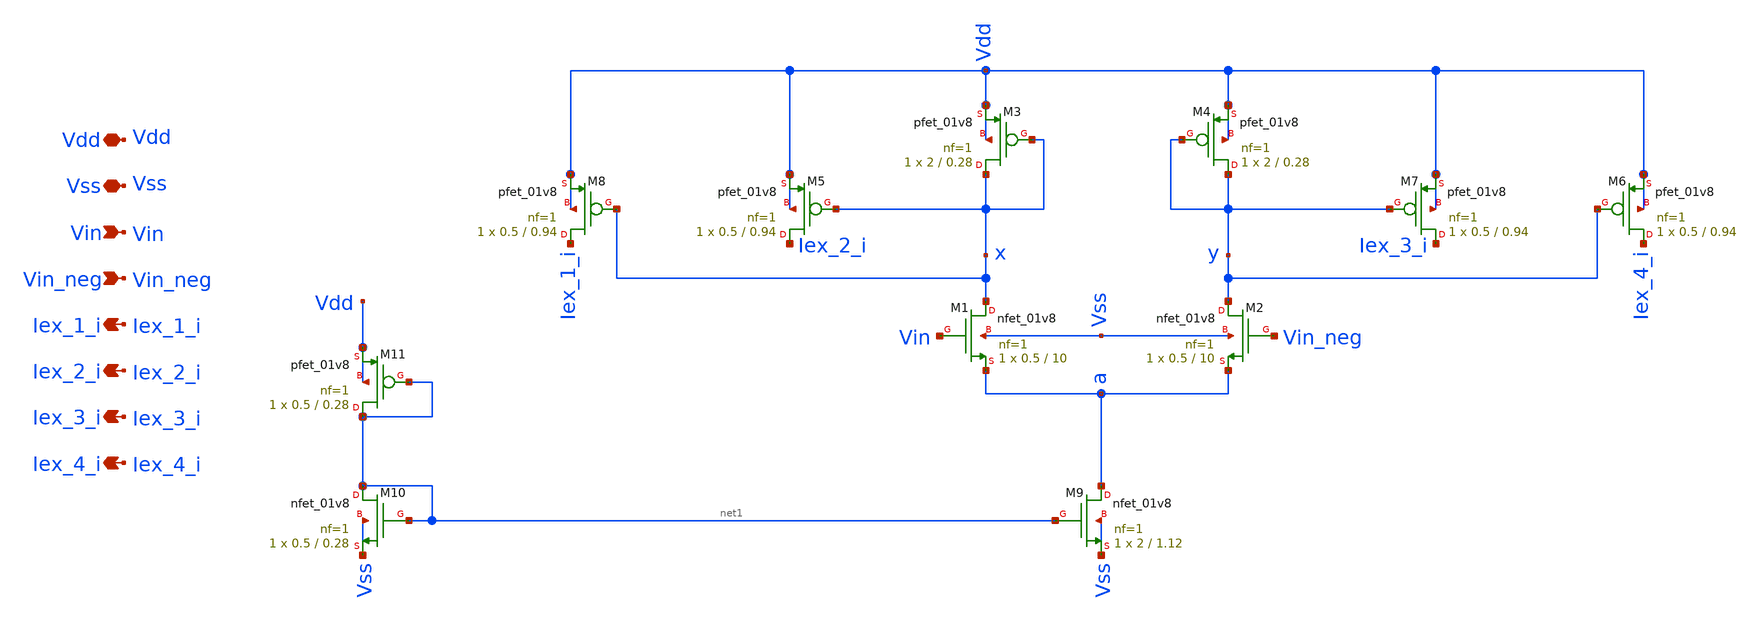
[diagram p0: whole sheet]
** sch_path: designs/libs/snn_analog/encoder/sch/encoder.sch
**.subckt encoder Vdd Vss Vin Vin_neg Iex_1_i Iex_4_i Iex_2_i Iex_3_i
*.iopin Vdd
*.iopin Vss
*.ipin Vin
*.ipin Vin_neg
*.opin Iex_1_i
*.opin Iex_4_i
*.opin Iex_2_i
*.opin Iex_3_i
XM1 x Vin a Vss sky130_fd_pr__nfet_01v8 L=10 W=0.5 nf=1 ad='int((1 + 1)/2) * 0.5 / 1 * 0.29' as='int((1 + 2)/2) * 0.5 / 1 * 0.29'
+ pd='2*int((1 + 1)/2) * (0.5 / 1 + 0.29)' ps='2*int((1 + 2)/2) * (0.5 / 1 + 0.29)' nrd='0.29 / 0.5 ' nrs='0.29 / 0.5 '
+ sa=0 sb=0 sd=0 mult=1 m=1
XM2 y Vin_neg a Vss sky130_fd_pr__nfet_01v8 L=10 W=0.5 nf=1 ad='int((1 + 1)/2) * 0.5 / 1 * 0.29' as='int((1 + 2)/2) * 0.5 / 1 * 0.29'
+ pd='2*int((1 + 1)/2) * (0.5 / 1 + 0.29)' ps='2*int((1 + 2)/2) * (0.5 / 1 + 0.29)' nrd='0.29 / 0.5 ' nrs='0.29 / 0.5 '
+ sa=0 sb=0 sd=0 mult=1 m=1
XM3 x x Vdd Vdd sky130_fd_pr__pfet_01v8 L=0.28 W=2 nf=1 ad='int((1 + 1)/2) * 2 / 1 * 0.29' as='int((1 + 2)/2) * 2 / 1 * 0.29'
+ pd='2*int((1 + 1)/2) * (2 / 1 + 0.29)' ps='2*int((1 + 2)/2) * (2 / 1 + 0.29)' nrd='0.29 / 2 ' nrs='0.29 / 2 '
+ sa=0 sb=0 sd=0 mult=1 m=1
XM4 y y Vdd Vdd sky130_fd_pr__pfet_01v8 L=0.28 W=2 nf=1 ad='int((1 + 1)/2) * 2 / 1 * 0.29' as='int((1 + 2)/2) * 2 / 1 * 0.29'
+ pd='2*int((1 + 1)/2) * (2 / 1 + 0.29)' ps='2*int((1 + 2)/2) * (2 / 1 + 0.29)' nrd='0.29 / 2 ' nrs='0.29 / 2 '
+ sa=0 sb=0 sd=0 mult=1 m=1
XM5 Iex_2_i x Vdd Vdd sky130_fd_pr__pfet_01v8 L=0.94 W=0.5 nf=1 ad='int((1 + 1)/2) * 0.5 / 1 * 0.29'
+ as='int((1 + 2)/2) * 0.5 / 1 * 0.29' pd='2*int((1 + 1)/2) * (0.5 / 1 + 0.29)' ps='2*int((1 + 2)/2) * (0.5 / 1 + 0.29)'
+ nrd='0.29 / 0.5 ' nrs='0.29 / 0.5 ' sa=0 sb=0 sd=0 mult=1 m=1
XM6 Iex_4_i y Vdd Vdd sky130_fd_pr__pfet_01v8 L=0.94 W=0.5 nf=1 ad='int((1 + 1)/2) * 0.5 / 1 * 0.29'
+ as='int((1 + 2)/2) * 0.5 / 1 * 0.29' pd='2*int((1 + 1)/2) * (0.5 / 1 + 0.29)' ps='2*int((1 + 2)/2) * (0.5 / 1 + 0.29)'
+ nrd='0.29 / 0.5 ' nrs='0.29 / 0.5 ' sa=0 sb=0 sd=0 mult=1 m=1
XM7 Iex_3_i y Vdd Vdd sky130_fd_pr__pfet_01v8 L=0.94 W=0.5 nf=1 ad='int((1 + 1)/2) * 0.5 / 1 * 0.29'
+ as='int((1 + 2)/2) * 0.5 / 1 * 0.29' pd='2*int((1 + 1)/2) * (0.5 / 1 + 0.29)' ps='2*int((1 + 2)/2) * (0.5 / 1 + 0.29)'
+ nrd='0.29 / 0.5 ' nrs='0.29 / 0.5 ' sa=0 sb=0 sd=0 mult=1 m=1
XM8 Iex_1_i x Vdd Vdd sky130_fd_pr__pfet_01v8 L=0.94 W=0.5 nf=1 ad='int((1 + 1)/2) * 0.5 / 1 * 0.29'
+ as='int((1 + 2)/2) * 0.5 / 1 * 0.29' pd='2*int((1 + 1)/2) * (0.5 / 1 + 0.29)' ps='2*int((1 + 2)/2) * (0.5 / 1 + 0.29)'
+ nrd='0.29 / 0.5 ' nrs='0.29 / 0.5 ' sa=0 sb=0 sd=0 mult=1 m=1
XM9 a net1 Vss Vss sky130_fd_pr__nfet_01v8 L=1.12 W=2 nf=1 ad='int((1 + 1)/2) * 2 / 1 * 0.29' as='int((1 + 2)/2) * 2 / 1 * 0.29'
+ pd='2*int((1 + 1)/2) * (2 / 1 + 0.29)' ps='2*int((1 + 2)/2) * (2 / 1 + 0.29)' nrd='0.29 / 2 ' nrs='0.29 / 2 '
+ sa=0 sb=0 sd=0 mult=1 m=1
XM10 net1 net1 Vss Vss sky130_fd_pr__nfet_01v8 L=0.28 W=0.5 nf=1 ad='int((1 + 1)/2) * 0.5 / 1 * 0.29'
+ as='int((1 + 2)/2) * 0.5 / 1 * 0.29' pd='2*int((1 + 1)/2) * (0.5 / 1 + 0.29)' ps='2*int((1 + 2)/2) * (0.5 / 1 + 0.29)'
+ nrd='0.29 / 0.5 ' nrs='0.29 / 0.5 ' sa=0 sb=0 sd=0 mult=1 m=1
XM11 net1 net1 Vdd Vdd sky130_fd_pr__pfet_01v8 L=0.28 W=0.5 nf=1 ad='int((1 + 1)/2) * 0.5 / 1 * 0.29'
+ as='int((1 + 2)/2) * 0.5 / 1 * 0.29' pd='2*int((1 + 1)/2) * (0.5 / 1 + 0.29)' ps='2*int((1 + 2)/2) * (0.5 / 1 + 0.29)'
+ nrd='0.29 / 0.5 ' nrs='0.29 / 0.5 ' sa=0 sb=0 sd=0 mult=1 m=1
**.ends
.end
